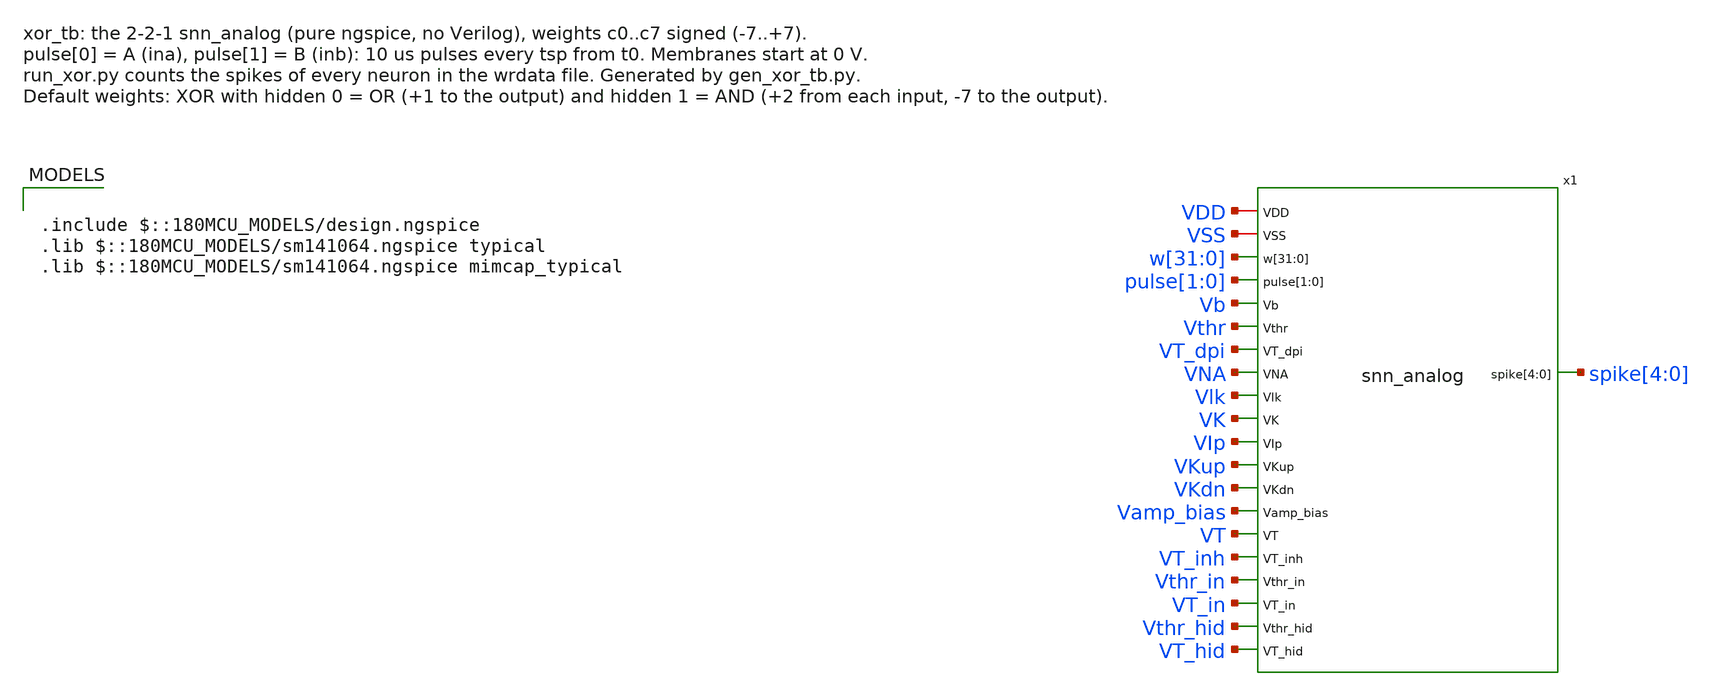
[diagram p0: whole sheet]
** sch_path: analog/testbenches/xor/xor_tb.sch
**.subckt xor_tb
x1 VDD VSS w[31] w[30] w[29] w[28] w[27] w[26] w[25] w[24] w[23] w[22] w[21] w[20] w[19] w[18] w[17]
+ w[16] w[15] w[14] w[13] w[12] w[11] w[10] w[9] w[8] w[7] w[6] w[5] w[4] w[3] w[2] w[1] w[0] pulse[1]
+ pulse[0] Vb Vthr VT_dpi VNA Vlk VK VIp VKup VKdn Vamp_bias VT VT_inh Vthr_in VT_in Vthr_hid VT_hid spike[4]
+ spike[3] spike[2] spike[1] spike[0] snn_analog
**** begin user architecture code

.include $::180MCU_MODELS/design.ngspice
.lib $::180MCU_MODELS/sm141064.ngspice typical
.lib $::180MCU_MODELS/sm141064.ngspice mimcap_typical


.param vdd=3.3 iref=14.42n
.param p_vthr=2.70 p_vtau=0.5096 p_vtau_i=0.5096
.param p_vthr_in=2.4 p_vtau_in=0.695 p_vthr_hid=2.5 p_vtau_hid=0.655
.param p_vlk=0.48 p_vamp_bias=0.535 p_vip=0.573 p_vna=1.93 p_vkup=2.35 p_vk=1.22 p_vkdn=0.588
+ p_vt=1.66
* Signed weights -7..+7, word k: 0, 1 pulse -> input; 2 + 2j + i input i -> hidden j; 6 + j hidden j
*+ -> output
.param c0=7 c1=7 c2=7 c3=7 c4=2 c5=2 c6=1 c7=-7
.param ina=1 inb=1 tpw=10u tsp=200u t0=100u tstop=4.1m
.csparam tstop_c={tstop}
Vdd VDD 0 {vdd}
Vss VSS 0 0
* DAC unit current: Iref into a diode-connected unit current source (w[0] = 15 nA)
Iref VDD Vb {iref}
XMref Vb Vb 0 0 nfet_03v3 L=8u W=1u nf=1
* VT_* are source-gate voltages of the DPI tau pFET (VT = VDD - p_vtau)
Vthr Vthr 0 {p_vthr}
Vtau VDD VT_dpi {p_vtau}
Vtau_i VDD VT_inh {p_vtau_i}
Vthr_in Vthr_in 0 {p_vthr_in}
Vtau_in VDD VT_in {p_vtau_in}
Vthr_hid Vthr_hid 0 {p_vthr_hid}
Vtau_hid VDD VT_hid {p_vtau_hid}
VNA VNA VSS {p_vna}
Vlk Vlk VSS {p_vlk}
VK VK VSS {p_vk}
VIp VIp VSS {p_vip}
VKup VKup VSS {p_vkup}
VKdn VKdn VSS {p_vkdn}
Vamp_bias Vamp_bias VSS {p_vamp_bias}
VT VT VSS {p_vt}
Vw0 w[0] 0 {vdd*(floor(abs(c0)/1)-2*floor(abs(c0)/2))}
Vw1 w[1] 0 {vdd*(floor(abs(c0)/2)-2*floor(abs(c0)/4))}
Vw2 w[2] 0 {vdd*(floor(abs(c0)/4)-2*floor(abs(c0)/8))}
Vw3 w[3] 0 {c0<0 ? vdd : 0}
Vw4 w[4] 0 {vdd*(floor(abs(c1)/1)-2*floor(abs(c1)/2))}
Vw5 w[5] 0 {vdd*(floor(abs(c1)/2)-2*floor(abs(c1)/4))}
Vw6 w[6] 0 {vdd*(floor(abs(c1)/4)-2*floor(abs(c1)/8))}
Vw7 w[7] 0 {c1<0 ? vdd : 0}
Vw8 w[8] 0 {vdd*(floor(abs(c2)/1)-2*floor(abs(c2)/2))}
Vw9 w[9] 0 {vdd*(floor(abs(c2)/2)-2*floor(abs(c2)/4))}
Vw10 w[10] 0 {vdd*(floor(abs(c2)/4)-2*floor(abs(c2)/8))}
Vw11 w[11] 0 {c2<0 ? vdd : 0}
Vw12 w[12] 0 {vdd*(floor(abs(c3)/1)-2*floor(abs(c3)/2))}
Vw13 w[13] 0 {vdd*(floor(abs(c3)/2)-2*floor(abs(c3)/4))}
Vw14 w[14] 0 {vdd*(floor(abs(c3)/4)-2*floor(abs(c3)/8))}
Vw15 w[15] 0 {c3<0 ? vdd : 0}
Vw16 w[16] 0 {vdd*(floor(abs(c4)/1)-2*floor(abs(c4)/2))}
Vw17 w[17] 0 {vdd*(floor(abs(c4)/2)-2*floor(abs(c4)/4))}
Vw18 w[18] 0 {vdd*(floor(abs(c4)/4)-2*floor(abs(c4)/8))}
Vw19 w[19] 0 {c4<0 ? vdd : 0}
Vw20 w[20] 0 {vdd*(floor(abs(c5)/1)-2*floor(abs(c5)/2))}
Vw21 w[21] 0 {vdd*(floor(abs(c5)/2)-2*floor(abs(c5)/4))}
Vw22 w[22] 0 {vdd*(floor(abs(c5)/4)-2*floor(abs(c5)/8))}
Vw23 w[23] 0 {c5<0 ? vdd : 0}
Vw24 w[24] 0 {vdd*(floor(abs(c6)/1)-2*floor(abs(c6)/2))}
Vw25 w[25] 0 {vdd*(floor(abs(c6)/2)-2*floor(abs(c6)/4))}
Vw26 w[26] 0 {vdd*(floor(abs(c6)/4)-2*floor(abs(c6)/8))}
Vw27 w[27] 0 {c6<0 ? vdd : 0}
Vw28 w[28] 0 {vdd*(floor(abs(c7)/1)-2*floor(abs(c7)/2))}
Vw29 w[29] 0 {vdd*(floor(abs(c7)/2)-2*floor(abs(c7)/4))}
Vw30 w[30] 0 {vdd*(floor(abs(c7)/4)-2*floor(abs(c7)/8))}
Vw31 w[31] 0 {c7<0 ? vdd : 0}
Vp0 pulse[0] 0 pulse(0 {vdd*ina} {t0} 10n 10n {tpw} {tsp})
Vp1 pulse[1] 0 pulse(0 {vdd*inb} {t0} 10n 10n {tpw} {tsp})
* spike[n] copied to sp<n> (no load) for wrdata
Esp0 sp0 0 spike[0] 0 1
Esp1 sp1 0 spike[1] 0 1
Esp2 sp2 0 spike[2] 0 1
Esp3 sp3 0 spike[3] 0 1
Esp4 sp4 0 spike[4] 0 1
.ic v(x1.VMEM_0)=0 v(x1.VMEM_1)=0 v(x1.VMEM_2)=0 v(x1.VMEM_3)=0 v(x1.VMEM_4)=0 v(spike[0])=0
+ v(spike[1])=0 v(spike[2])=0 v(spike[3])=0 v(spike[4])=0
.options method=gear

.control
  save v(sp0) v(sp1) v(sp2) v(sp3) v(sp4) v(x1.VMEM_0) v(x1.VMEM_1) v(x1.VMEM_2) v(x1.VMEM_3)
+ v(x1.VMEM_4)
  set wr_singlescale
  set wr_vecnames
  * Max step 0.1u: at 0.5u a relay spike edge sometimes kicked a neuron into a false spike
  tran 0.1u $&tstop_c 0 0.1u
  meas tran vmax_out max v(x1.VMEM_4)
  echo RES vmax_out=$&vmax_out
  wrdata xor_tb.txt v(sp0) v(sp1) v(sp2) v(sp3) v(sp4) v(x1.VMEM_0) v(x1.VMEM_1) v(x1.VMEM_2)
+ v(x1.VMEM_3) v(x1.VMEM_4)
  if $?batchmode = 0
    plot v(x1.VMEM_4) v(sp4)+4 v(sp2)*0.3+8 v(sp3)*0.3+9.5 v(sp0)*0.3+11 v(sp1)*0.3+12.5 title 'Output membrane, output spike; hidden OR, AND; inputs A, B (offset)'
+ ylabel 'V'
  end
.endc


**** end user architecture code
**.ends
.end
